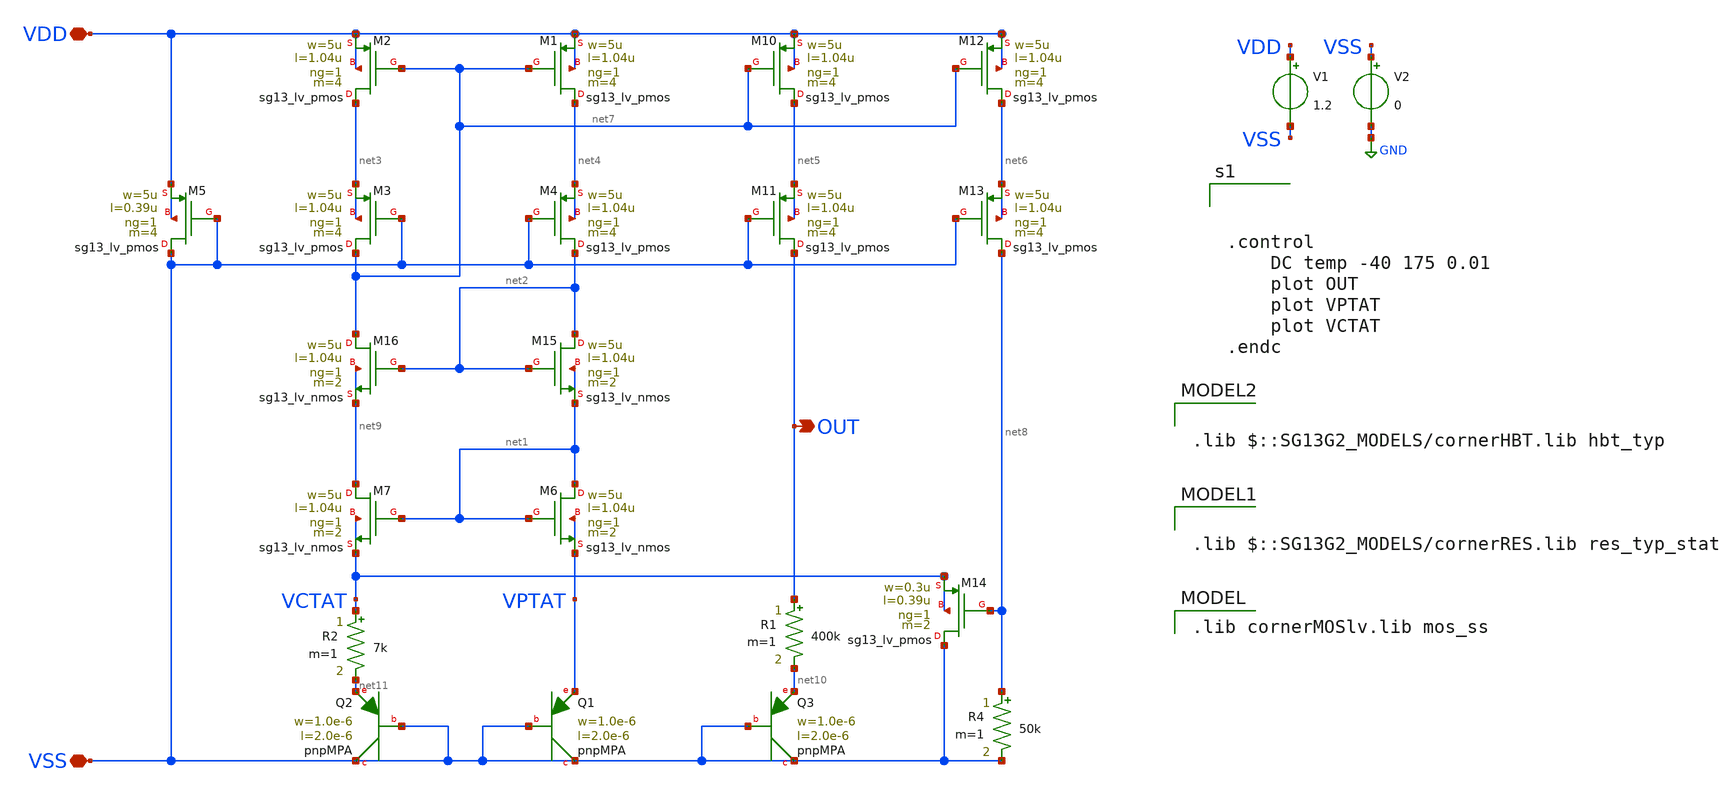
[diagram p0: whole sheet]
** sch_path: libs/core_analog/core_bandgap/testbench/psrr_bandgap.sch
**.subckt psrr_bandgap VDD VSS OUT
*.iopin VDD
*.iopin VSS
*.opin OUT
XM1 net4 net7 VDD VDD sg13_lv_pmos w=5u l=1.04u ng=1 m=4 mm_ok=1
XM2 net3 net7 VDD VDD sg13_lv_pmos w=5u l=1.04u ng=1 m=4 mm_ok=1
XM3 net7 VSS net3 net3 sg13_lv_pmos w=5u l=1.04u ng=1 m=4 mm_ok=1
XM4 net2 VSS net4 net4 sg13_lv_pmos w=5u l=1.04u ng=1 m=4 mm_ok=1
XM5 VSS VSS VDD VDD sg13_lv_pmos w=5u l=0.39u ng=1 m=4 mm_ok=1
XM10 net5 net7 VDD VDD sg13_lv_pmos w=5u l=1.04u ng=1 m=4 mm_ok=1
XM11 OUT VSS net5 net5 sg13_lv_pmos w=5u l=1.04u ng=1 m=4 mm_ok=1
XM12 net6 net7 VDD VDD sg13_lv_pmos w=5u l=1.04u ng=1 m=4 mm_ok=1
XM13 net8 VSS net6 net6 sg13_lv_pmos w=5u l=1.04u ng=1 m=4 mm_ok=1
XQ1 VSS VSS VPTAT pnpMPA a=2p p=6u m=1
XQ2 VSS VSS net11 pnpMPA a=2p p=6u m=8
XQ3 VSS VSS net10 pnpMPA a=2p p=6u m=1
XM14 VSS net8 VCTAT VCTAT sg13_lv_pmos w=0.3u l=0.39u ng=1 m=2 mm_ok=1
XM15 net2 net2 net1 net1 sg13_lv_nmos w=5u l=1.04u ng=1 m=2 mm_ok=1
XM16 net7 net2 net9 net9 sg13_lv_nmos w=5u l=1.04u ng=1 m=2 mm_ok=1
XM6 net1 net1 VPTAT VPTAT sg13_lv_nmos w=5u l=1.04u ng=1 m=2 mm_ok=1
XM7 net9 net1 VCTAT VCTAT sg13_lv_nmos w=5u l=1.04u ng=1 m=2 mm_ok=1
V1 VDD VSS 1.2
V2 VSS GND 0
R4 net8 VSS 50k m=1
R1 OUT net10 400k m=1
R2 VCTAT net11 7k m=1
**** begin user architecture code



.control
	DC temp -40 175 0.01
	plot OUT
	plot VPTAT
	plot VCTAT
.endc


 .lib cornerMOSlv.lib mos_ss


.lib $::SG13G2_MODELS/cornerRES.lib res_typ_stat


.lib $::SG13G2_MODELS/cornerHBT.lib hbt_typ

**** end user architecture code
**.ends
.GLOBAL GND
.end
